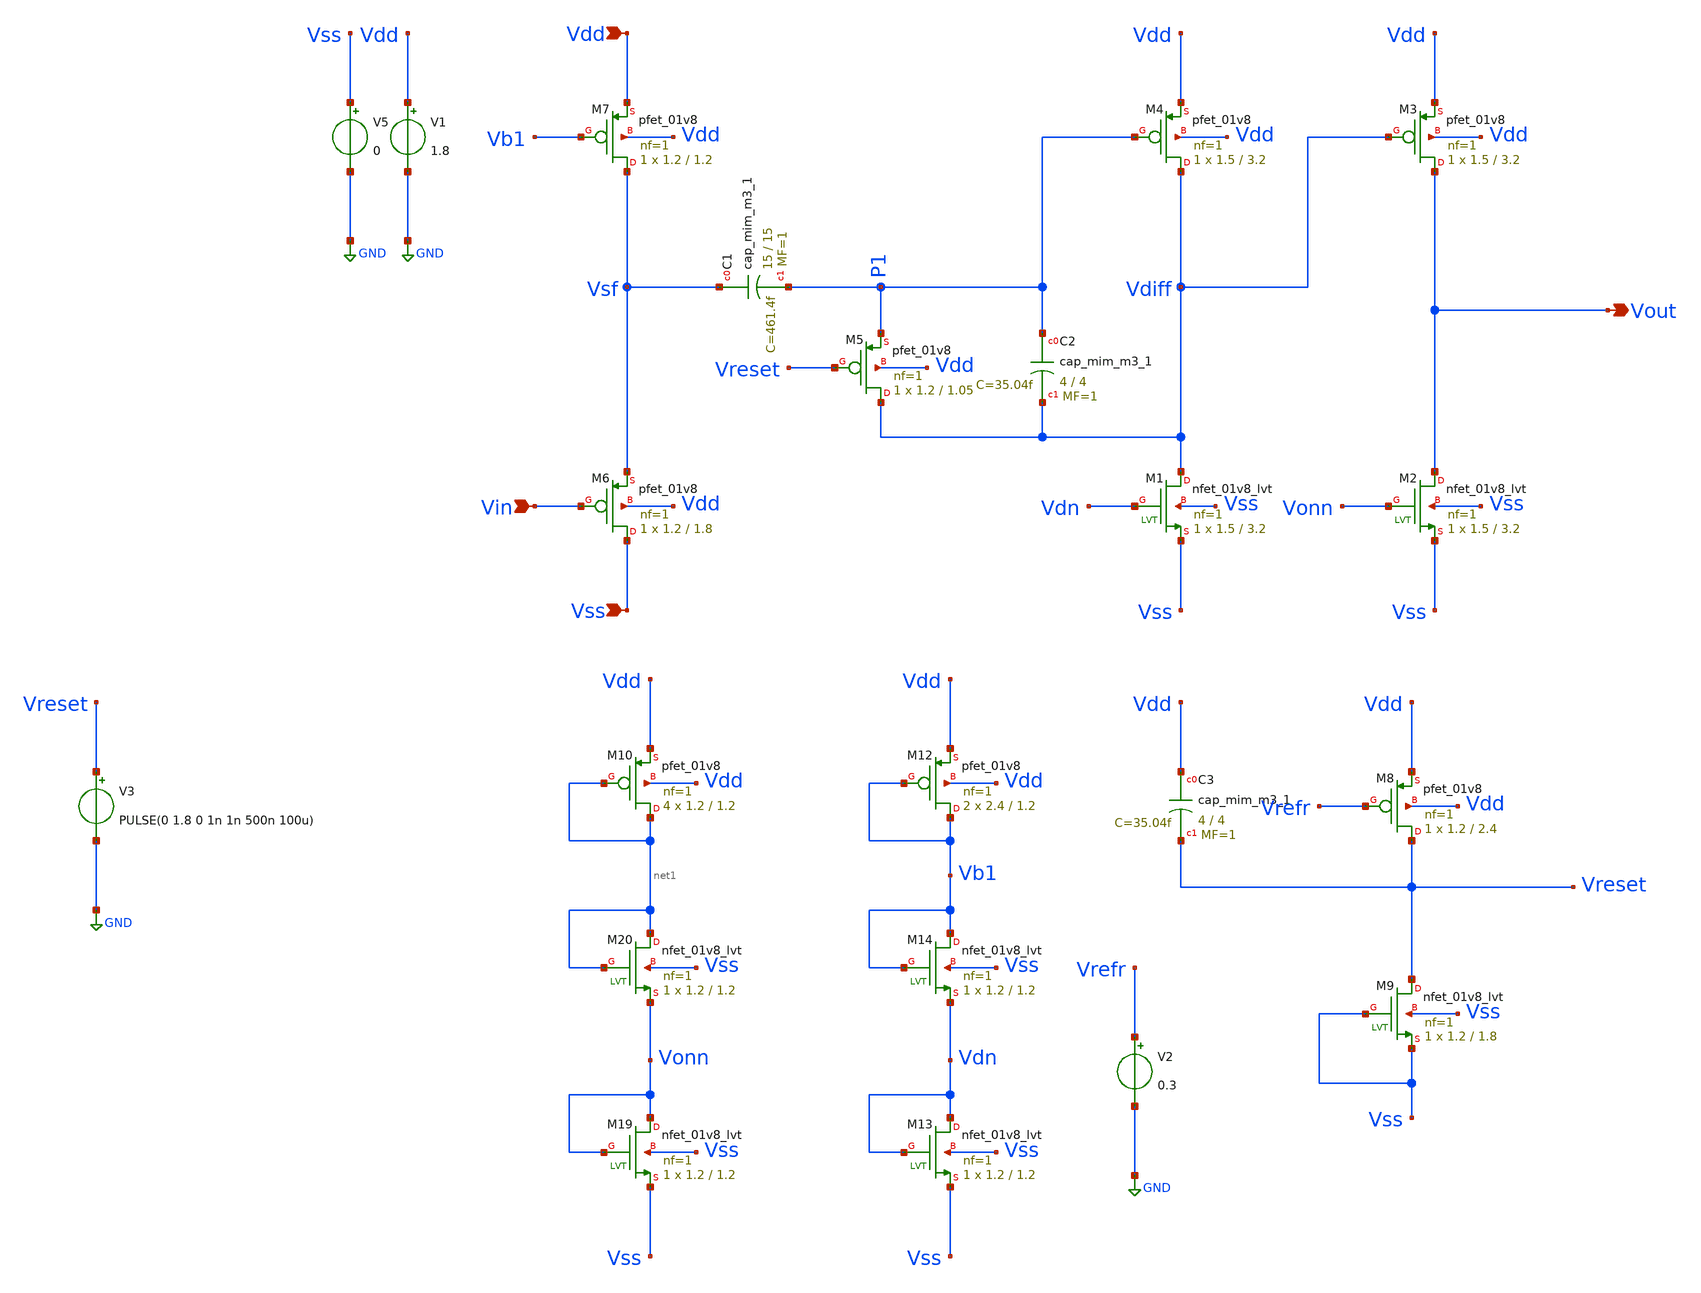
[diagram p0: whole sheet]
** sch_path: testbenches/ATS_V0.1_tb.sch
**.subckt ATS_V0.1_tb Vdd Vss Vin Vout
*.ipin Vdd
*.ipin Vss
*.ipin Vin
*.opin Vout
XM3 Vout Vdiff Vdd Vdd sky130_fd_pr__pfet_01v8 L=3.2 W=1.5 nf=1 ad='int((nf+1)/2) * W/nf * 0.29' as='int((nf+2)/2) * W/nf * 0.29'
+ pd='2*int((nf+1)/2) * (W/nf + 0.29)' ps='2*int((nf+2)/2) * (W/nf + 0.29)' nrd='0.29 / W' nrs='0.29 / W'
+ sa=0 sb=0 sd=0 mult=1 m=1
XM4 Vdiff P1 Vdd Vdd sky130_fd_pr__pfet_01v8 L=3.2 W=1.5 nf=1 ad='int((nf+1)/2) * W/nf * 0.29' as='int((nf+2)/2) * W/nf * 0.29'
+ pd='2*int((nf+1)/2) * (W/nf + 0.29)' ps='2*int((nf+2)/2) * (W/nf + 0.29)' nrd='0.29 / W' nrs='0.29 / W'
+ sa=0 sb=0 sd=0 mult=1 m=1
XM5 Vdiff Vreset P1 Vdd sky130_fd_pr__pfet_01v8 L=1.05 W=1.2 nf=1 ad='int((nf+1)/2) * W/nf * 0.29' as='int((nf+2)/2) * W/nf * 0.29'
+ pd='2*int((nf+1)/2) * (W/nf + 0.29)' ps='2*int((nf+2)/2) * (W/nf + 0.29)' nrd='0.29 / W' nrs='0.29 / W'
+ sa=0 sb=0 sd=0 mult=1 m=1
XM6 Vss Vin Vsf Vdd sky130_fd_pr__pfet_01v8 L=1.8 W=1.2 nf=1 ad='int((nf+1)/2) * W/nf * 0.29' as='int((nf+2)/2) * W/nf * 0.29'
+ pd='2*int((nf+1)/2) * (W/nf + 0.29)' ps='2*int((nf+2)/2) * (W/nf + 0.29)' nrd='0.29 / W' nrs='0.29 / W'
+ sa=0 sb=0 sd=0 mult=1 m=1
XM7 Vsf Vb1 Vdd Vdd sky130_fd_pr__pfet_01v8 L=1.2 W=1.2 nf=1 ad='int((nf+1)/2) * W/nf * 0.29' as='int((nf+2)/2) * W/nf * 0.29'
+ pd='2*int((nf+1)/2) * (W/nf + 0.29)' ps='2*int((nf+2)/2) * (W/nf + 0.29)' nrd='0.29 / W' nrs='0.29 / W'
+ sa=0 sb=0 sd=0 mult=1 m=1
XC1 Vsf P1 sky130_fd_pr__cap_mim_m3_1 W=15 L=15 MF=1 m=1
XC2 P1 Vdiff sky130_fd_pr__cap_mim_m3_1 W=4 L=4 MF=1 m=1
V1 Vdd GND 1.8
V5 Vss GND 0
XM1 Vdiff Vdn Vss Vss sky130_fd_pr__nfet_01v8_lvt L=3.2 W=1.5 nf=1 ad='int((nf+1)/2) * W/nf * 0.29' as='int((nf+2)/2) * W/nf * 0.29'
+ pd='2*int((nf+1)/2) * (W/nf + 0.29)' ps='2*int((nf+2)/2) * (W/nf + 0.29)' nrd='0.29 / W' nrs='0.29 / W'
+ sa=0 sb=0 sd=0 mult=1 m=1
XM2 Vout Vonn Vss Vss sky130_fd_pr__nfet_01v8_lvt L=3.2 W=1.5 nf=1 ad='int((nf+1)/2) * W/nf * 0.29' as='int((nf+2)/2) * W/nf * 0.29'
+ pd='2*int((nf+1)/2) * (W/nf + 0.29)' ps='2*int((nf+2)/2) * (W/nf + 0.29)' nrd='0.29 / W' nrs='0.29 / W'
+ sa=0 sb=0 sd=0 mult=1 m=1
XM8 Vreset Vrefr Vdd Vdd sky130_fd_pr__pfet_01v8 L=2.4 W=1.2 nf=1 ad='int((nf+1)/2) * W/nf * 0.29' as='int((nf+2)/2) * W/nf * 0.29'
+ pd='2*int((nf+1)/2) * (W/nf + 0.29)' ps='2*int((nf+2)/2) * (W/nf + 0.29)' nrd='0.29 / W' nrs='0.29 / W'
+ sa=0 sb=0 sd=0 mult=1 m=1
XM9 Vreset Vss Vss Vss sky130_fd_pr__nfet_01v8_lvt L=1.8 W=1.2 nf=1 ad='int((nf+1)/2) * W/nf * 0.29'
+ as='int((nf+2)/2) * W/nf * 0.29' pd='2*int((nf+1)/2) * (W/nf + 0.29)' ps='2*int((nf+2)/2) * (W/nf + 0.29)'
+ nrd='0.29 / W' nrs='0.29 / W' sa=0 sb=0 sd=0 mult=1 m=1
XC3 Vdd Vreset sky130_fd_pr__cap_mim_m3_1 W=4 L=4 MF=1 m=1
XM12 Vb1 Vb1 Vdd Vdd sky130_fd_pr__pfet_01v8 L=1.2 W=2.4 nf=1 ad='int((nf+1)/2) * W/nf * 0.29' as='int((nf+2)/2) * W/nf * 0.29'
+ pd='2*int((nf+1)/2) * (W/nf + 0.29)' ps='2*int((nf+2)/2) * (W/nf + 0.29)' nrd='0.29 / W' nrs='0.29 / W'
+ sa=0 sb=0 sd=0 mult=2 m=2
XM13 Vdn Vdn Vss Vss sky130_fd_pr__nfet_01v8_lvt L=1.2 W=1.2 nf=1 ad='int((nf+1)/2) * W/nf * 0.29' as='int((nf+2)/2) * W/nf * 0.29'
+ pd='2*int((nf+1)/2) * (W/nf + 0.29)' ps='2*int((nf+2)/2) * (W/nf + 0.29)' nrd='0.29 / W' nrs='0.29 / W'
+ sa=0 sb=0 sd=0 mult=1 m=1
XM14 Vb1 Vb1 Vdn Vss sky130_fd_pr__nfet_01v8_lvt L=1.2 W=1.2 nf=1 ad='int((nf+1)/2) * W/nf * 0.29' as='int((nf+2)/2) * W/nf * 0.29'
+ pd='2*int((nf+1)/2) * (W/nf + 0.29)' ps='2*int((nf+2)/2) * (W/nf + 0.29)' nrd='0.29 / W' nrs='0.29 / W'
+ sa=0 sb=0 sd=0 mult=1 m=1
XM19 Vonn Vonn Vss Vss sky130_fd_pr__nfet_01v8_lvt L=1.2 W=1.2 nf=1 ad='int((nf+1)/2) * W/nf * 0.29'
+ as='int((nf+2)/2) * W/nf * 0.29' pd='2*int((nf+1)/2) * (W/nf + 0.29)' ps='2*int((nf+2)/2) * (W/nf + 0.29)'
+ nrd='0.29 / W' nrs='0.29 / W' sa=0 sb=0 sd=0 mult=1 m=1
XM20 net1 net1 Vonn Vss sky130_fd_pr__nfet_01v8_lvt L=1.2 W=1.2 nf=1 ad='int((nf+1)/2) * W/nf * 0.29'
+ as='int((nf+2)/2) * W/nf * 0.29' pd='2*int((nf+1)/2) * (W/nf + 0.29)' ps='2*int((nf+2)/2) * (W/nf + 0.29)'
+ nrd='0.29 / W' nrs='0.29 / W' sa=0 sb=0 sd=0 mult=1 m=1
XM10 net1 net1 Vdd Vdd sky130_fd_pr__pfet_01v8 L=1.2 W=1.2 nf=1 ad='int((nf+1)/2) * W/nf * 0.29' as='int((nf+2)/2) * W/nf * 0.29'
+ pd='2*int((nf+1)/2) * (W/nf + 0.29)' ps='2*int((nf+2)/2) * (W/nf + 0.29)' nrd='0.29 / W' nrs='0.29 / W'
+ sa=0 sb=0 sd=0 mult=4 m=4
V2 Vrefr GND 0.3
V3 Vreset GND PULSE(0 1.8 0 1n 1n 500n 100u)
**** begin user architecture code

** opencircuitdesign pdks install
.lib $::SKYWATER_MODELS/sky130.lib.spice tt

*.include /foss/designs/Analog_to_Spike/version_0.0/sym.spice





.option savecurrents
.temp 27

* Case #1 -> 100 Hz
Vin vin 0 SIN(0 0.8 100 0 0)
*Vin1 n2 n1 SIN(0 0.8 150 0 0)
*Vin2 n3 n1 SIN(0 0.9 250 0 0)
*Vin4 vin n3 SIN(0 0.6 200 0 0)
*Vreset vreset 0 PULSE(1.8 0 0 1u 1u 900u 1000u)

* Case #2 -> 10 Hz
*Vin vin 0 SIN(-0.5 1.8 10 0 0)
*Vreset vreset 0 PULSE(1.8 0 0 100u 100u 9m 10m)

* Case #3 -> 1 Hz
*Vin vin 0 SIN(0 1.8 1 0 0)
*Vin vin 0 PULSE(0 0.8 0 100m 1 1 2)
*Vreset vreset 0 PULSE(1.8 0 0 1m 1m 90m 100m)

.control
save all
*op

* Case #1 -> Run 40 ms
tran 1u 0.04

* Case #2 -> Run 400 ms
*tran 100u 0.4

* Case #3 -> Run 4 s
*tran 1m 10

plot vin vdiff vsf

write ATS_V0.1.raw

.endc



**** end user architecture code
**.ends
.GLOBAL GND
.end
